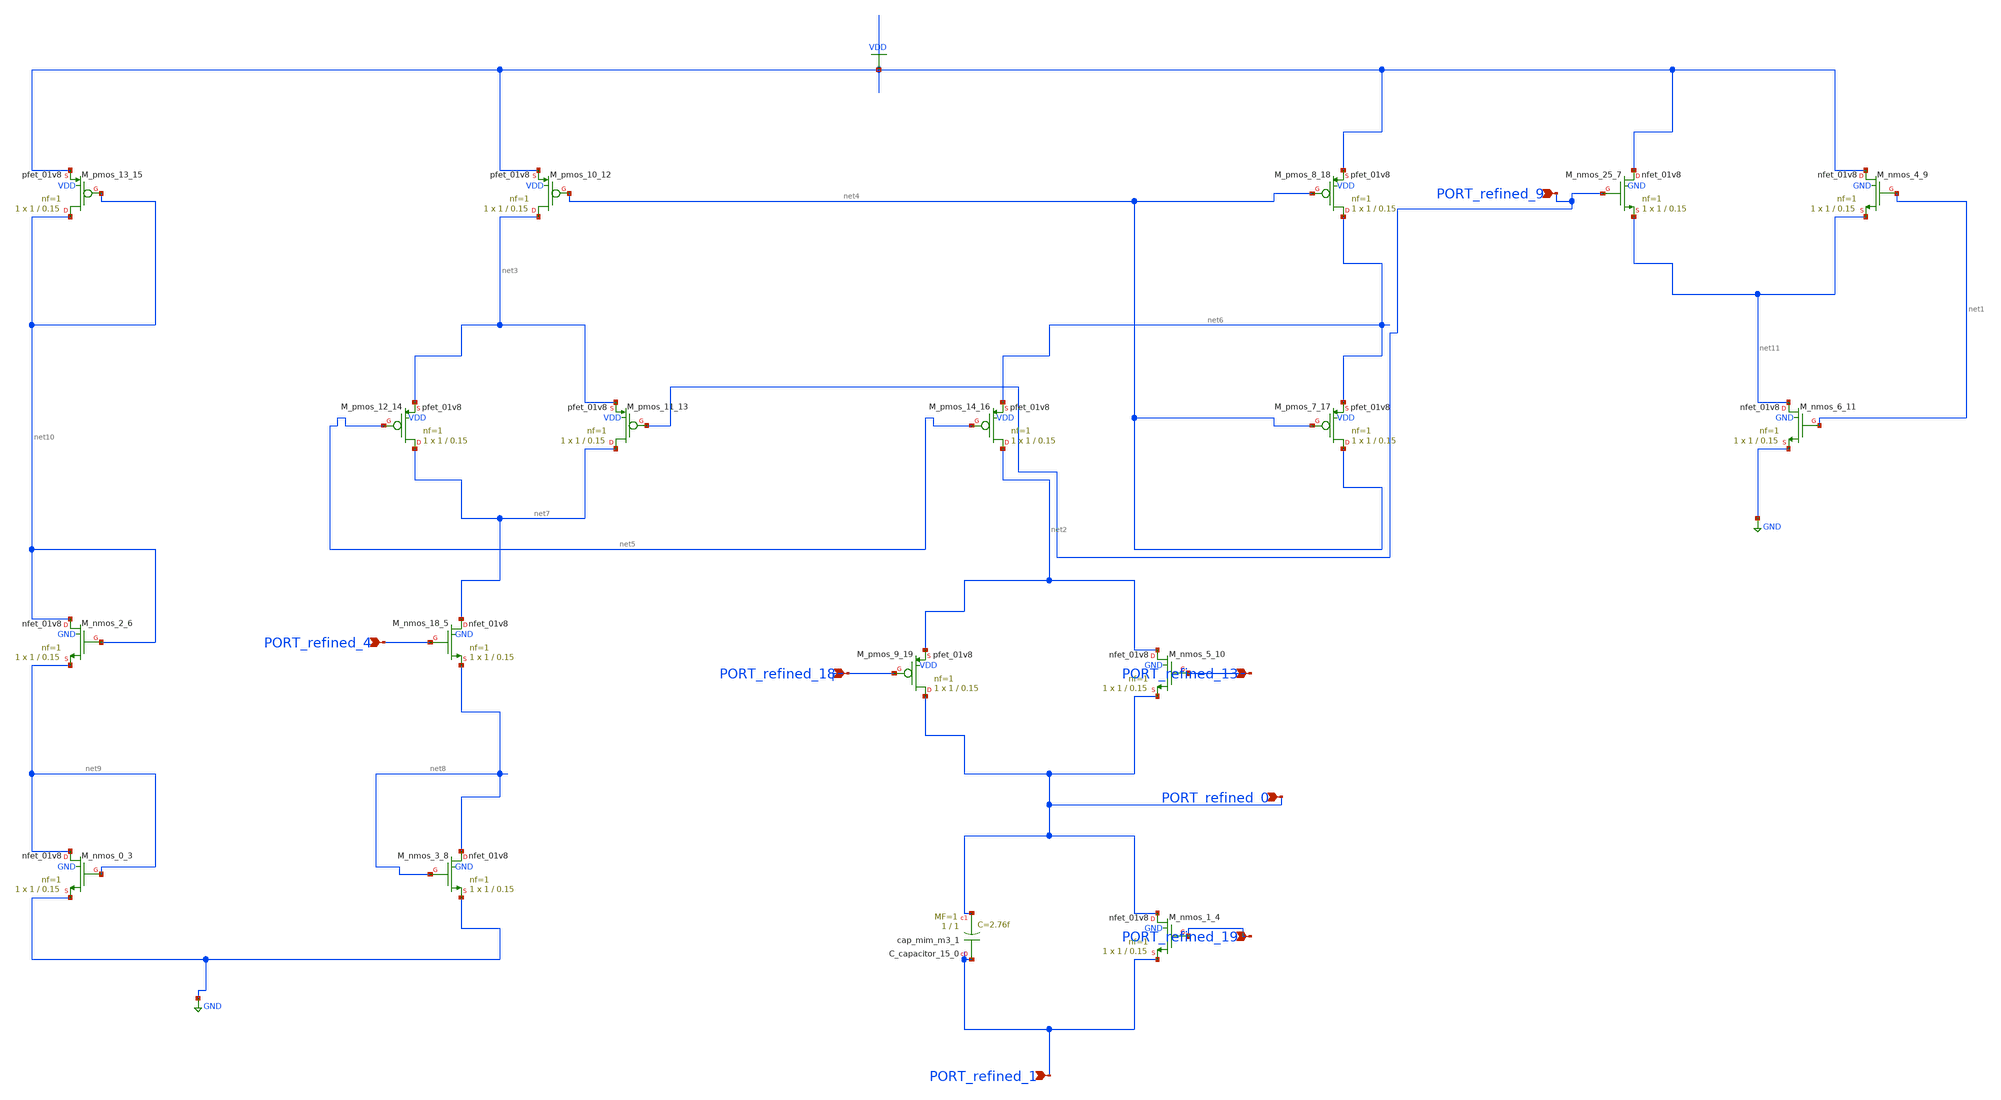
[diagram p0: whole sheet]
** sch_path: schematics/SchemGen/10_1038_s41598-025-17286-6_13_001.sch
**.subckt 10_1038_s41598-025-17286-6_13_001 PORT_refined_4 PORT_refined_19 PORT_refined_0
*+ PORT_refined_13 PORT_refined_9 PORT_refined_1 PORT_refined_18
*.ipin PORT_refined_4
*.ipin PORT_refined_19
*.ipin PORT_refined_0
*.ipin PORT_refined_13
*.ipin PORT_refined_9
*.ipin PORT_refined_1
*.ipin PORT_refined_18
XC_capacitor_15_0 PORT_refined_1 PORT_refined_0 sky130_fd_pr__cap_mim_m3_1 W=1 L=1 MF=1 m=1
XM_nmos_0_3 net9 net9 GND GND sky130_fd_pr__nfet_01v8 L=0.15 W=1 nf=1 ad='int((1 + 1)/2) * 1 / 1 * 0.29'
+ as='int((1 + 2)/2) * 1 / 1 * 0.29' pd='2*int((1 + 1)/2) * (1 / 1 + 0.29)' ps='2*int((1 + 2)/2) * (1 / 1 + 0.29)'
+ nrd='0.29 / 1 ' nrs='0.29 / 1 ' sa=0 sb=0 sd=0 mult=1 m=1
XM_nmos_1_4 PORT_refined_0 PORT_refined_19 PORT_refined_1 GND sky130_fd_pr__nfet_01v8 L=0.15 W=1 nf=1
+ ad='int((1 + 1)/2) * 1 / 1 * 0.29' as='int((1 + 2)/2) * 1 / 1 * 0.29' pd='2*int((1 + 1)/2) * (1 / 1 + 0.29)'
+ ps='2*int((1 + 2)/2) * (1 / 1 + 0.29)' nrd='0.29 / 1 ' nrs='0.29 / 1 ' sa=0 sb=0 sd=0 mult=1 m=1
XM_nmos_18_5 net7 PORT_refined_4 net8 GND sky130_fd_pr__nfet_01v8 L=0.15 W=1 nf=1 ad='int((1 + 1)/2) * 1 / 1 * 0.29'
+ as='int((1 + 2)/2) * 1 / 1 * 0.29' pd='2*int((1 + 1)/2) * (1 / 1 + 0.29)' ps='2*int((1 + 2)/2) * (1 / 1 + 0.29)'
+ nrd='0.29 / 1 ' nrs='0.29 / 1 ' sa=0 sb=0 sd=0 mult=1 m=1
XM_nmos_2_6 net10 net10 net9 GND sky130_fd_pr__nfet_01v8 L=0.15 W=1 nf=1 ad='int((1 + 1)/2) * 1 / 1 * 0.29'
+ as='int((1 + 2)/2) * 1 / 1 * 0.29' pd='2*int((1 + 1)/2) * (1 / 1 + 0.29)' ps='2*int((1 + 2)/2) * (1 / 1 + 0.29)'
+ nrd='0.29 / 1 ' nrs='0.29 / 1 ' sa=0 sb=0 sd=0 mult=1 m=1
XM_nmos_25_7 VDD PORT_refined_9 net11 GND sky130_fd_pr__nfet_01v8 L=0.15 W=1 nf=1 ad='int((1 + 1)/2) * 1 / 1 * 0.29'
+ as='int((1 + 2)/2) * 1 / 1 * 0.29' pd='2*int((1 + 1)/2) * (1 / 1 + 0.29)' ps='2*int((1 + 2)/2) * (1 / 1 + 0.29)'
+ nrd='0.29 / 1 ' nrs='0.29 / 1 ' sa=0 sb=0 sd=0 mult=1 m=1
XM_nmos_3_8 net8 net8 GND GND sky130_fd_pr__nfet_01v8 L=0.15 W=1 nf=1 ad='int((1 + 1)/2) * 1 / 1 * 0.29'
+ as='int((1 + 2)/2) * 1 / 1 * 0.29' pd='2*int((1 + 1)/2) * (1 / 1 + 0.29)' ps='2*int((1 + 2)/2) * (1 / 1 + 0.29)'
+ nrd='0.29 / 1 ' nrs='0.29 / 1 ' sa=0 sb=0 sd=0 mult=1 m=1
XM_nmos_4_9 VDD net1 net11 GND sky130_fd_pr__nfet_01v8 L=0.15 W=1 nf=1 ad='int((1 + 1)/2) * 1 / 1 * 0.29'
+ as='int((1 + 2)/2) * 1 / 1 * 0.29' pd='2*int((1 + 1)/2) * (1 / 1 + 0.29)' ps='2*int((1 + 2)/2) * (1 / 1 + 0.29)'
+ nrd='0.29 / 1 ' nrs='0.29 / 1 ' sa=0 sb=0 sd=0 mult=1 m=1
XM_nmos_5_10 net2 PORT_refined_13 PORT_refined_0 GND sky130_fd_pr__nfet_01v8 L=0.15 W=1 nf=1 ad='int((1 + 1)/2) * 1 / 1 * 0.29'
+ as='int((1 + 2)/2) * 1 / 1 * 0.29' pd='2*int((1 + 1)/2) * (1 / 1 + 0.29)' ps='2*int((1 + 2)/2) * (1 / 1 + 0.29)'
+ nrd='0.29 / 1 ' nrs='0.29 / 1 ' sa=0 sb=0 sd=0 mult=1 m=1
XM_nmos_6_11 net11 net1 GND GND sky130_fd_pr__nfet_01v8 L=0.15 W=1 nf=1 ad='int((1 + 1)/2) * 1 / 1 * 0.29'
+ as='int((1 + 2)/2) * 1 / 1 * 0.29' pd='2*int((1 + 1)/2) * (1 / 1 + 0.29)' ps='2*int((1 + 2)/2) * (1 / 1 + 0.29)'
+ nrd='0.29 / 1 ' nrs='0.29 / 1 ' sa=0 sb=0 sd=0 mult=1 m=1
XM_pmos_10_12 net3 net4 VDD VDD sky130_fd_pr__pfet_01v8 L=0.15 W=1 nf=1 ad='int((1 + 1)/2) * 1 / 1 * 0.29'
+ as='int((1 + 2)/2) * 1 / 1 * 0.29' pd='2*int((1 + 1)/2) * (1 / 1 + 0.29)' ps='2*int((1 + 2)/2) * (1 / 1 + 0.29)'
+ nrd='0.29 / 1 ' nrs='0.29 / 1 ' sa=0 sb=0 sd=0 mult=1 m=1
XM_pmos_11_13 net7 PORT_refined_9 net3 VDD sky130_fd_pr__pfet_01v8 L=0.15 W=1 nf=1 ad='int((1 + 1)/2) * 1 / 1 * 0.29'
+ as='int((1 + 2)/2) * 1 / 1 * 0.29' pd='2*int((1 + 1)/2) * (1 / 1 + 0.29)' ps='2*int((1 + 2)/2) * (1 / 1 + 0.29)'
+ nrd='0.29 / 1 ' nrs='0.29 / 1 ' sa=0 sb=0 sd=0 mult=1 m=1
XM_pmos_12_14 net7 net5 net3 VDD sky130_fd_pr__pfet_01v8 L=0.15 W=1 nf=1 ad='int((1 + 1)/2) * 1 / 1 * 0.29'
+ as='int((1 + 2)/2) * 1 / 1 * 0.29' pd='2*int((1 + 1)/2) * (1 / 1 + 0.29)' ps='2*int((1 + 2)/2) * (1 / 1 + 0.29)'
+ nrd='0.29 / 1 ' nrs='0.29 / 1 ' sa=0 sb=0 sd=0 mult=1 m=1
XM_pmos_13_15 net10 net10 VDD VDD sky130_fd_pr__pfet_01v8 L=0.15 W=1 nf=1 ad='int((1 + 1)/2) * 1 / 1 * 0.29'
+ as='int((1 + 2)/2) * 1 / 1 * 0.29' pd='2*int((1 + 1)/2) * (1 / 1 + 0.29)' ps='2*int((1 + 2)/2) * (1 / 1 + 0.29)'
+ nrd='0.29 / 1 ' nrs='0.29 / 1 ' sa=0 sb=0 sd=0 mult=1 m=1
XM_pmos_14_16 net2 net5 net6 VDD sky130_fd_pr__pfet_01v8 L=0.15 W=1 nf=1 ad='int((1 + 1)/2) * 1 / 1 * 0.29'
+ as='int((1 + 2)/2) * 1 / 1 * 0.29' pd='2*int((1 + 1)/2) * (1 / 1 + 0.29)' ps='2*int((1 + 2)/2) * (1 / 1 + 0.29)'
+ nrd='0.29 / 1 ' nrs='0.29 / 1 ' sa=0 sb=0 sd=0 mult=1 m=1
XM_pmos_7_17 net4 net4 net6 VDD sky130_fd_pr__pfet_01v8 L=0.15 W=1 nf=1 ad='int((1 + 1)/2) * 1 / 1 * 0.29'
+ as='int((1 + 2)/2) * 1 / 1 * 0.29' pd='2*int((1 + 1)/2) * (1 / 1 + 0.29)' ps='2*int((1 + 2)/2) * (1 / 1 + 0.29)'
+ nrd='0.29 / 1 ' nrs='0.29 / 1 ' sa=0 sb=0 sd=0 mult=1 m=1
XM_pmos_8_18 net6 net4 VDD VDD sky130_fd_pr__pfet_01v8 L=0.15 W=1 nf=1 ad='int((1 + 1)/2) * 1 / 1 * 0.29'
+ as='int((1 + 2)/2) * 1 / 1 * 0.29' pd='2*int((1 + 1)/2) * (1 / 1 + 0.29)' ps='2*int((1 + 2)/2) * (1 / 1 + 0.29)'
+ nrd='0.29 / 1 ' nrs='0.29 / 1 ' sa=0 sb=0 sd=0 mult=1 m=1
XM_pmos_9_19 PORT_refined_0 PORT_refined_18 net2 VDD sky130_fd_pr__pfet_01v8 L=0.15 W=1 nf=1 ad='int((1 + 1)/2) * 1 / 1 * 0.29'
+ as='int((1 + 2)/2) * 1 / 1 * 0.29' pd='2*int((1 + 1)/2) * (1 / 1 + 0.29)' ps='2*int((1 + 2)/2) * (1 / 1 + 0.29)'
+ nrd='0.29 / 1 ' nrs='0.29 / 1 ' sa=0 sb=0 sd=0 mult=1 m=1
**.ends
.GLOBAL GND
.GLOBAL VDD
.end
